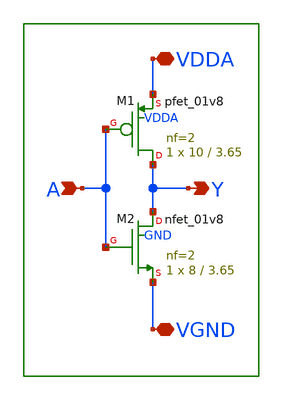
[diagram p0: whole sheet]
** sch_path: xschem/lib/old_main_inv.sch
**.subckt old_main_inv VDDA VGND A Y
*.iopin VDDA
*.iopin VGND
*.ipin A
*.opin Y
XM1 Y A VDDA VDDA sky130_fd_pr__pfet_01v8 L=3.65 W=10 nf=2 ad='int((2 + 1)/2) * 10 / 2 * 0.29' as='int((2 + 2)/2) * 10 / 2 * 0.29'
+ pd='2*int((2 + 1)/2) * (10 / 2 + 0.29)' ps='2*int((2 + 2)/2) * (10 / 2 + 0.29)' nrd='0.29 / 10 ' nrs='0.29 / 10 '
+ sa=0 sb=0 sd=0 mult=1 m=1
XM2 Y A VGND GND sky130_fd_pr__nfet_01v8 L=3.65 W=8 nf=2 ad='int((nf+1)/2) * W/nf * 0.29' as='int((nf+2)/2) * W/nf * 0.29'
+ pd='2*int((nf+1)/2) * (W/nf + 0.29)' ps='2*int((nf+2)/2) * (W/nf + 0.29)' nrd='0.29 / W' nrs='0.29 / W'
+ sa=0 sb=0 sd=0 mult=1 m=1
**.ends
.end
